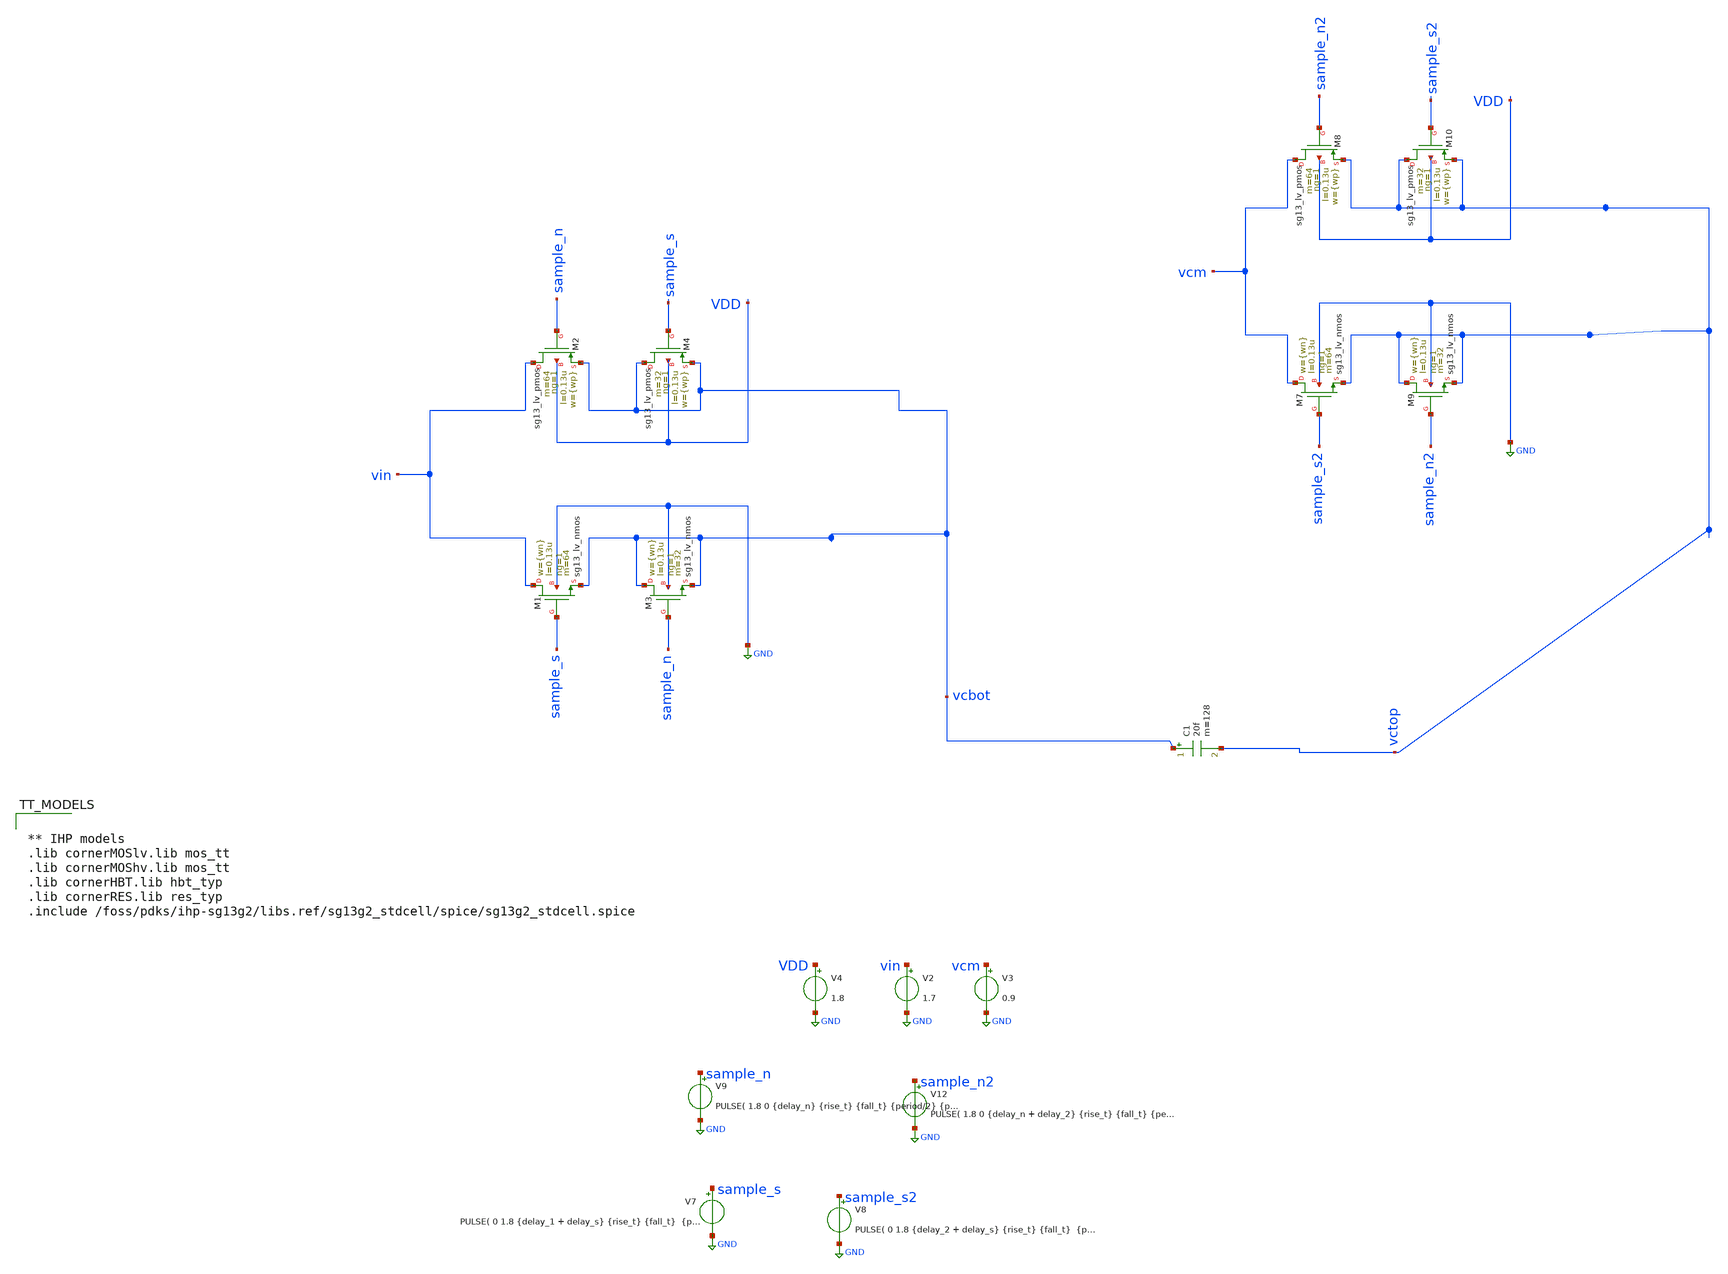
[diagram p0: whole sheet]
** sch_path: xschem/dac_icms_cell_ideall/testbenches/tb_capacitor_tgate_time.sch
**.subckt tb_capacitor_tgate_time
V7 sample_s GND PULSE( 0 1.8 {delay_1 + delay_s} {rise_t} {fall_t} {period/2} {period} 1)
V2 vin GND 1.7
V3 vcm GND 0.9
V4 VDD GND 1.8
C1 vcbot vctop 20f m=128
XM1 vin sample_s vcbot GND sg13_lv_nmos w={wn} l=0.13u ng=1 m=64 mm_ok=1
XM2 vin sample_n vcbot VDD sg13_lv_pmos w={wp} l=0.13u ng=1 m=64 mm_ok=1
XM3 vcbot sample_n vcbot GND sg13_lv_nmos w={wn} l=0.13u ng=1 m=32 mm_ok=1
XM4 vcbot sample_s vcbot VDD sg13_lv_pmos w={wp} l=0.13u ng=1 m=32 mm_ok=1
XM7 vcm sample_s2 vctop GND sg13_lv_nmos w={wn} l=0.13u ng=1 m=64 mm_ok=1
XM8 vcm sample_n2 vctop VDD sg13_lv_pmos w={wp} l=0.13u ng=1 m=64 mm_ok=1
XM9 vctop sample_n2 vctop GND sg13_lv_nmos w={wn} l=0.13u ng=1 m=32 mm_ok=1
XM10 vctop sample_s2 vctop VDD sg13_lv_pmos w={wp} l=0.13u ng=1 m=32 mm_ok=1
V8 sample_s2 GND PULSE( 0 1.8 {delay_2 + delay_s} {rise_t} {fall_t} {period/2} {period} 1)
V9 sample_n GND PULSE( 1.8 0 {delay_n} {rise_t} {fall_t} {period/2} {period} 1)
V12 sample_n2 GND PULSE( 1.8 0 {delay_n + delay_2} {rise_t} {fall_t} {period/2} {period} 1)
**** begin user architecture code


.param temp=27
.param period = 1n
.param wp = 1u
.param wn = 1u
.param rise_t = period*0.05
.param fall_t = period*0.05
.param delay_n = 0
.param delay_s = 0
.param delay_2 = period*0.2
.param delay_1 = 0
.options savecurrents klu method=gear reltol=1e-2 abstol=1e-15 gmin=1e-10
.control

* Transient Analysis
tran 1p 2n

*plot {d0} {d1 + 4} {d2 + 8} {d3 + 12} {d4 + 16} {d5 + 20} {d6 + 24} {d7 + 28} {d8 + 32} {d9 + 36} {d10 + 40}
*+ {d11 + 44}
*plot {b0} {b1 + 4} {b2 + 8} {b3 + 12} {b4 + 16} {b5 + 20} {b6 + 24} {b7 + 28} {b8 + 32} {b9 + 36} {b10 + 40}
*+ {b11 + 44}
*plot {clk} {comp_in + 2} {sample + 4}
plot vctop vcbot sample_s
plot {vctop-vcbot} sample_s
plot i(v1) i(v5)
*plot x3.x14.net1-vctop x3.x18.vcap-vcbot
plot sample_s sample_n sample_s2+2 sample_n2+2
.endc




** IHP models
.lib cornerMOSlv.lib mos_tt
.lib cornerMOShv.lib mos_tt
.lib cornerHBT.lib hbt_typ
.lib cornerRES.lib res_typ
.include /foss/pdks/ihp-sg13g2/libs.ref/sg13g2_stdcell/spice/sg13g2_stdcell.spice


**** end user architecture code
**.ends
.GLOBAL GND
.end
